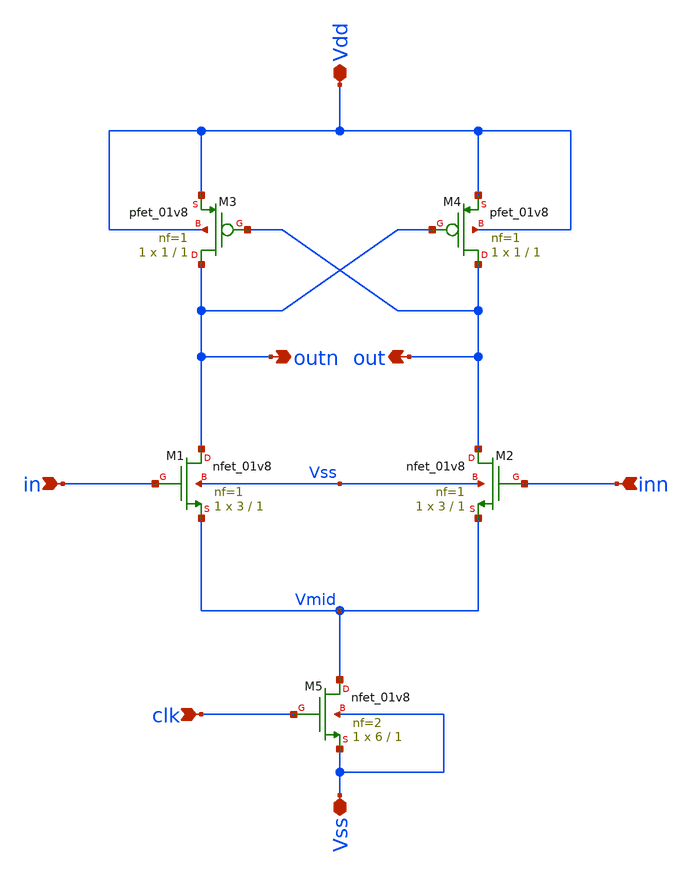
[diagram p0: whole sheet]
** sch_path: Circuits/Examples/Latch/CCLatch.sch
**.subckt CCLatch Vdd Vss in inn clk outn out
*.iopin Vdd
*.iopin Vss
*.ipin in
*.ipin inn
*.ipin clk
*.opin outn
*.opin out
XM1 outn in Vmid Vss sky130_fd_pr__nfet_01v8 L=1 W=3 nf=1 ad='int((nf+1)/2) * W/nf * 0.29' as='int((nf+2)/2) * W/nf * 0.29'
+ pd='2*int((nf+1)/2) * (W/nf + 0.29)' ps='2*int((nf+2)/2) * (W/nf + 0.29)' nrd='0.29 / W' nrs='0.29 / W'
+ sa=0 sb=0 sd=0 mult=1 m=1
XM2 out inn Vmid Vss sky130_fd_pr__nfet_01v8 L=1 W=3 nf=1 ad='int((nf+1)/2) * W/nf * 0.29' as='int((nf+2)/2) * W/nf * 0.29'
+ pd='2*int((nf+1)/2) * (W/nf + 0.29)' ps='2*int((nf+2)/2) * (W/nf + 0.29)' nrd='0.29 / W' nrs='0.29 / W'
+ sa=0 sb=0 sd=0 mult=1 m=1
XM3 outn out Vdd Vdd sky130_fd_pr__pfet_01v8 L=1 W=1 nf=1 ad='int((nf+1)/2) * W/nf * 0.29' as='int((nf+2)/2) * W/nf * 0.29'
+ pd='2*int((nf+1)/2) * (W/nf + 0.29)' ps='2*int((nf+2)/2) * (W/nf + 0.29)' nrd='0.29 / W' nrs='0.29 / W'
+ sa=0 sb=0 sd=0 mult=1 m=1
XM4 out outn Vdd Vdd sky130_fd_pr__pfet_01v8 L=1 W=1 nf=1 ad='int((nf+1)/2) * W/nf * 0.29' as='int((nf+2)/2) * W/nf * 0.29'
+ pd='2*int((nf+1)/2) * (W/nf + 0.29)' ps='2*int((nf+2)/2) * (W/nf + 0.29)' nrd='0.29 / W' nrs='0.29 / W'
+ sa=0 sb=0 sd=0 mult=1 m=1
XM5 Vmid clk Vss Vss sky130_fd_pr__nfet_01v8 L=1 W=6 nf=2 ad='int((nf+1)/2) * W/nf * 0.29' as='int((nf+2)/2) * W/nf * 0.29'
+ pd='2*int((nf+1)/2) * (W/nf + 0.29)' ps='2*int((nf+2)/2) * (W/nf + 0.29)' nrd='0.29 / W' nrs='0.29 / W'
+ sa=0 sb=0 sd=0 mult=1 m=1
**.ends
.end
